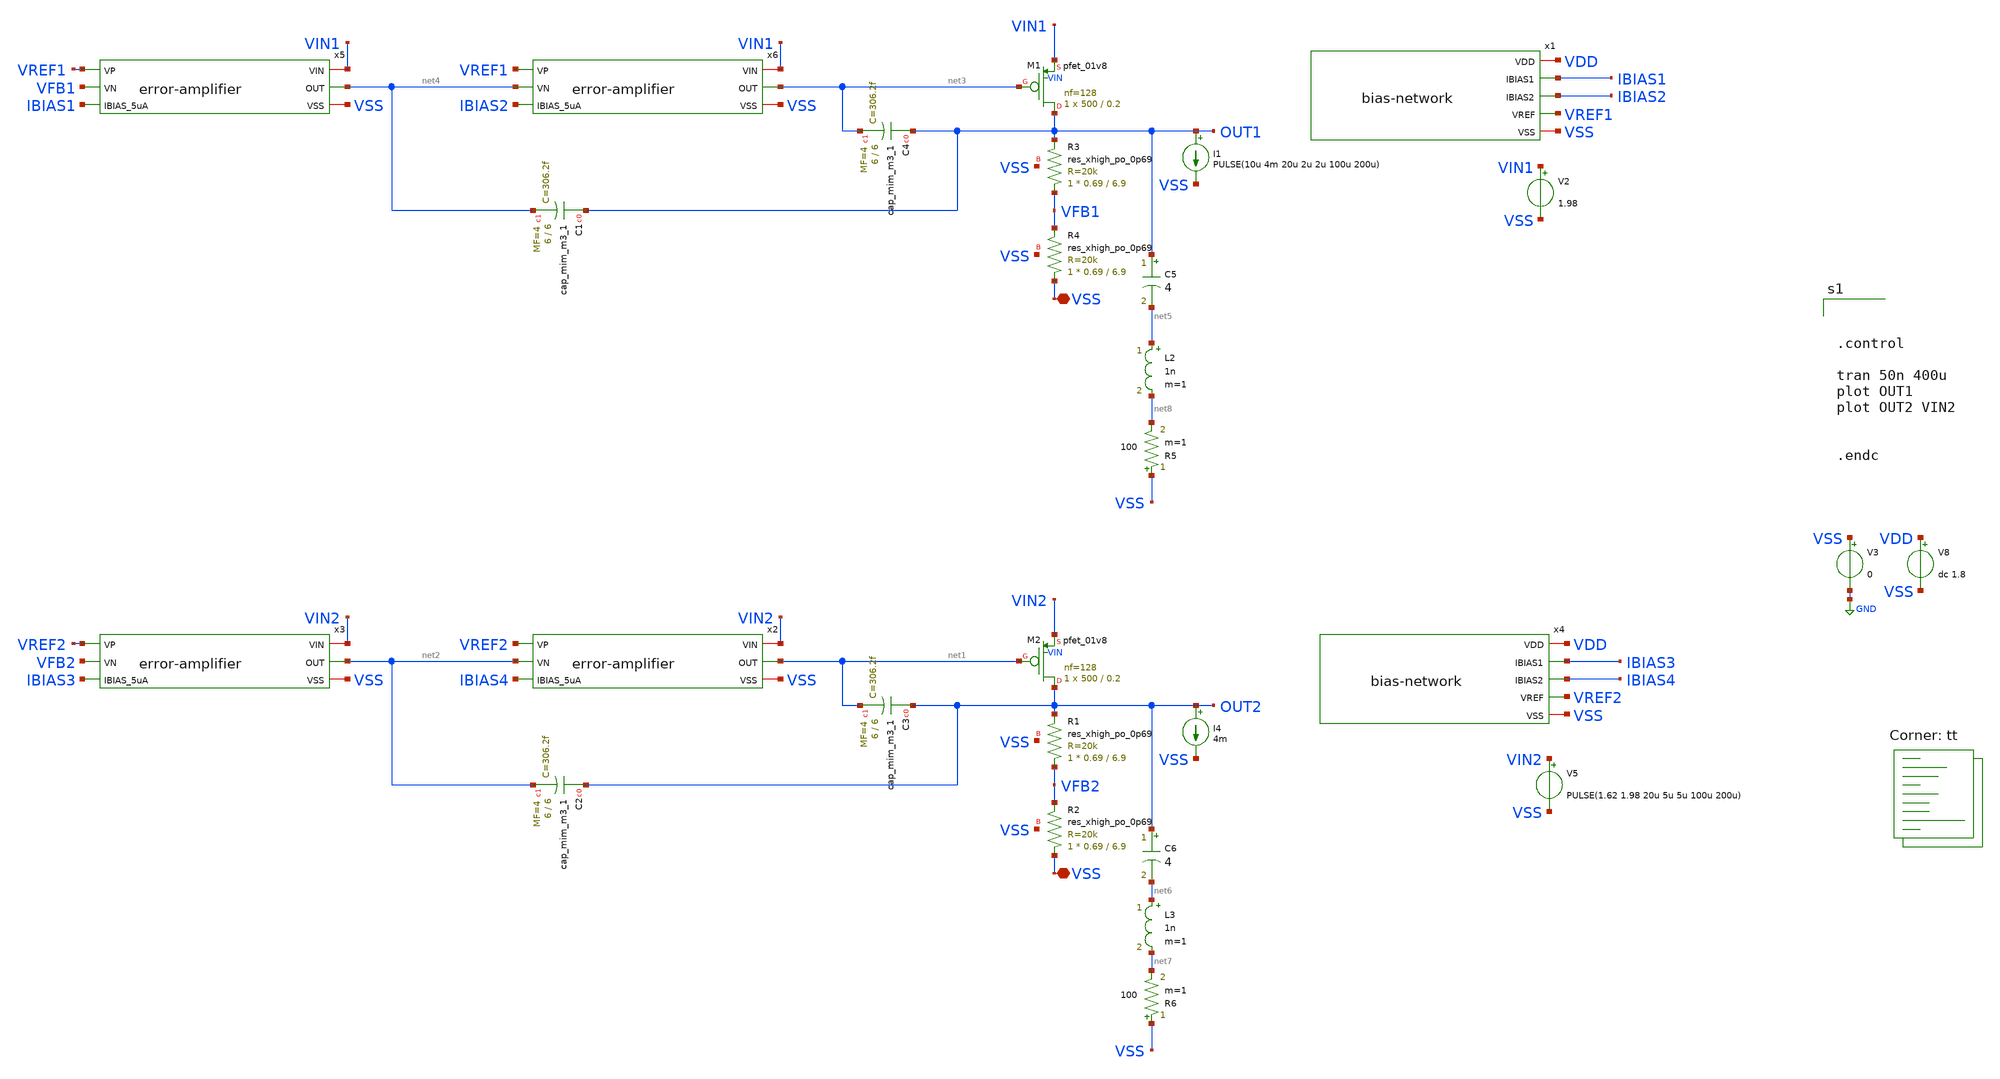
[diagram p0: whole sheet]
** sch_path: xschem/ldo_andriansyah/testbench/line-load-transient.sch
**.subckt line-load-transient VSS VSS
*.iopin VSS
*.iopin VSS
V2 VIN1 VSS 1.98
V3 VSS GND 0
I1 OUT1 VSS PULSE(10u 4m 20u 2u 2u 100u 200u)
V5 VIN2 VSS PULSE(1.62 1.98 20u 5u 5u 100u 200u)
I4 OUT2 VSS 4m
XC2 OUT2 net2 sky130_fd_pr__cap_mim_m3_1 W=6 L=6 MF=4 m=4
XC3 OUT2 net1 sky130_fd_pr__cap_mim_m3_1 W=6 L=6 MF=4 m=4
x3 VIN2 VREF2 VFB2 IBIAS3 net2 VSS error-amplifier
XR1 VFB2 OUT2 VSS sky130_fd_pr__res_xhigh_po_0p69 L=6.9 mult=1 m=1
XR2 VSS VFB2 VSS sky130_fd_pr__res_xhigh_po_0p69 L=6.9 mult=1 m=1
XM2 OUT2 net1 VIN2 VIN sky130_fd_pr__pfet_01v8 L=0.2 W=500 nf=128 ad='int((nf+1)/2) * W/nf * 0.29' as='int((nf+2)/2) * W/nf * 0.29'
+ pd='2*int((nf+1)/2) * (W/nf + 0.29)' ps='2*int((nf+2)/2) * (W/nf + 0.29)' nrd='0.29 / W' nrs='0.29 / W'
+ sa=0 sb=0 sd=0 mult=1 m=1
x2 VIN2 VREF2 net2 IBIAS4 net1 VSS error-amplifier
XC1 OUT1 net4 sky130_fd_pr__cap_mim_m3_1 W=6 L=6 MF=4 m=4
XC4 OUT1 net3 sky130_fd_pr__cap_mim_m3_1 W=6 L=6 MF=4 m=4
x5 VIN1 VREF1 VFB1 IBIAS1 net4 VSS error-amplifier
XR3 VFB1 OUT1 VSS sky130_fd_pr__res_xhigh_po_0p69 L=6.9 mult=1 m=1
XR4 VSS VFB1 VSS sky130_fd_pr__res_xhigh_po_0p69 L=6.9 mult=1 m=1
XM1 OUT1 net3 VIN1 VIN sky130_fd_pr__pfet_01v8 L=0.2 W=500 nf=128 ad='int((nf+1)/2) * W/nf * 0.29' as='int((nf+2)/2) * W/nf * 0.29'
+ pd='2*int((nf+1)/2) * (W/nf + 0.29)' ps='2*int((nf+2)/2) * (W/nf + 0.29)' nrd='0.29 / W' nrs='0.29 / W'
+ sa=0 sb=0 sd=0 mult=1 m=1
x6 VIN1 VREF1 net4 IBIAS2 net3 VSS error-amplifier
x1 VDD IBIAS1 IBIAS2 VREF1 VSS bias-network
x4 VDD IBIAS3 IBIAS4 VREF2 VSS bias-network
V8 VDD VSS dc 1.8
R5 VSS net8 100 m=1
C5 OUT1 net5 4 m=1
R6 VSS net7 100 m=1
C6 OUT2 net6 4 m=1
L2 net5 net8 1n m=1
L3 net6 net7 1n m=1
**** begin user architecture code



.control

tran 50n 400u
plot OUT1
plot OUT2 VIN2


.endc




.lib $::SKYWATER_MODELS/sky130.lib.spice tt
**** end user architecture code
**.ends

* expanding   symbol:
*+  /foss/designs/2026/tt_sky26b_ldo_andriansyah/xschem/error-amplifier/error-amplifier.sym # of pins=6
** sym_path: xschem/error-amplifier/error-amplifier.sym
** sch_path: xschem/error-amplifier/error-amplifier.sch
.subckt error-amplifier VIN VP VN IBIAS_5uA OUT VSS
*.ipin IBIAS_5uA
*.ipin VN
*.ipin VP
*.iopin VIN
*.iopin VSS
*.opin OUT
XM1 net2 net2 VSS VSS sky130_fd_pr__nfet_01v8 L=0.6 W=4.2 nf=4 ad='int((nf+1)/2) * W/nf * 0.29' as='int((nf+2)/2) * W/nf * 0.29'
+ pd='2*int((nf+1)/2) * (W/nf + 0.29)' ps='2*int((nf+2)/2) * (W/nf + 0.29)' nrd='0.29 / W' nrs='0.29 / W'
+ sa=0 sb=0 sd=0 mult=1 m=1
XM2 OUT net2 VSS VSS sky130_fd_pr__nfet_01v8 L=0.6 W=4.2 nf=4 ad='int((nf+1)/2) * W/nf * 0.29' as='int((nf+2)/2) * W/nf * 0.29'
+ pd='2*int((nf+1)/2) * (W/nf + 0.29)' ps='2*int((nf+2)/2) * (W/nf + 0.29)' nrd='0.29 / W' nrs='0.29 / W'
+ sa=0 sb=0 sd=0 mult=1 m=1
XM3 net2 VN net1 VIN sky130_fd_pr__pfet_01v8 L=0.6 W=28 nf=4 ad='int((nf+1)/2) * W/nf * 0.29' as='int((nf+2)/2) * W/nf * 0.29'
+ pd='2*int((nf+1)/2) * (W/nf + 0.29)' ps='2*int((nf+2)/2) * (W/nf + 0.29)' nrd='0.29 / W' nrs='0.29 / W'
+ sa=0 sb=0 sd=0 mult=1 m=1
XM4 OUT VP net1 VIN sky130_fd_pr__pfet_01v8 L=0.6 W=28 nf=4 ad='int((nf+1)/2) * W/nf * 0.29' as='int((nf+2)/2) * W/nf * 0.29'
+ pd='2*int((nf+1)/2) * (W/nf + 0.29)' ps='2*int((nf+2)/2) * (W/nf + 0.29)' nrd='0.29 / W' nrs='0.29 / W'
+ sa=0 sb=0 sd=0 mult=1 m=1
XM5 net1 IBIAS_5uA VIN VIN sky130_fd_pr__pfet_01v8 L=0.6 W=6.6 nf=4 ad='int((nf+1)/2) * W/nf * 0.29'
+ as='int((nf+2)/2) * W/nf * 0.29' pd='2*int((nf+1)/2) * (W/nf + 0.29)' ps='2*int((nf+2)/2) * (W/nf + 0.29)'
+ nrd='0.29 / W' nrs='0.29 / W' sa=0 sb=0 sd=0 mult=1 m=1
XM6 IBIAS_5uA IBIAS_5uA VIN VIN sky130_fd_pr__pfet_01v8 L=0.6 W=6.6 nf=4 ad='int((nf+1)/2) * W/nf * 0.29'
+ as='int((nf+2)/2) * W/nf * 0.29' pd='2*int((nf+1)/2) * (W/nf + 0.29)' ps='2*int((nf+2)/2) * (W/nf + 0.29)'
+ nrd='0.29 / W' nrs='0.29 / W' sa=0 sb=0 sd=0 mult=1 m=1
.ends


* expanding   symbol:
*+  /foss/designs/2026/tt_sky26b_ldo_andriansyah/xschem/bias-net/schematics/bias-network.sym # of pins=5
** sym_path: xschem/bias-net/schematics/bias-network.sym
** sch_path: xschem/bias-net/schematics/bias-network.sch
.subckt bias-network VDD IBIAS1 IBIAS2 VREF VSS
*.iopin VDD
*.iopin VSS
*.opin IBIAS1
*.opin IBIAS2
*.opin VREF
XM2 VREF VREF VSS VSS sky130_fd_pr__nfet_01v8 L=2 W=3 nf=4 ad='int((nf+1)/2) * W/nf * 0.29' as='int((nf+2)/2) * W/nf * 0.29'
+ pd='2*int((nf+1)/2) * (W/nf + 0.29)' ps='2*int((nf+2)/2) * (W/nf + 0.29)' nrd='0.29 / W' nrs='0.29 / W'
+ sa=0 sb=0 sd=0 mult=2 m=2
XR1 VREF net1 VSS sky130_fd_pr__res_xhigh_po_0p69 L=6.9 mult=1 m=1
XR2 net2 net1 VSS sky130_fd_pr__res_xhigh_po_0p69 L=6.9 mult=1 m=1
XR3 net2 net3 VSS sky130_fd_pr__res_xhigh_po_0p69 L=6.9 mult=1 m=1
XR4 net4 net3 VSS sky130_fd_pr__res_xhigh_po_0p69 L=6.9 mult=1 m=1
XR5 net4 net5 VSS sky130_fd_pr__res_xhigh_po_0p69 L=6.9 mult=1 m=1
XR6 net9 net10 VSS sky130_fd_pr__res_xhigh_po_0p69 L=6.9 mult=1 m=1
XR7 net9 net8 VSS sky130_fd_pr__res_xhigh_po_0p69 L=6.9 mult=1 m=1
XR8 net7 net8 VSS sky130_fd_pr__res_xhigh_po_0p69 L=6.9 mult=1 m=1
XR9 net7 net6 VSS sky130_fd_pr__res_xhigh_po_0p69 L=6.9 mult=1 m=1
XR10 net5 net6 VSS sky130_fd_pr__res_xhigh_po_0p69 L=6.9 mult=1 m=1
XM1 IBIAS1 VREF VSS VSS sky130_fd_pr__nfet_01v8 L=2 W=3 nf=4 ad='int((nf+1)/2) * W/nf * 0.29' as='int((nf+2)/2) * W/nf * 0.29'
+ pd='2*int((nf+1)/2) * (W/nf + 0.29)' ps='2*int((nf+2)/2) * (W/nf + 0.29)' nrd='0.29 / W' nrs='0.29 / W'
+ sa=0 sb=0 sd=0 mult=2 m=2
XM3 IBIAS2 VREF VSS VSS sky130_fd_pr__nfet_01v8 L=2 W=3 nf=4 ad='int((nf+1)/2) * W/nf * 0.29' as='int((nf+2)/2) * W/nf * 0.29'
+ pd='2*int((nf+1)/2) * (W/nf + 0.29)' ps='2*int((nf+2)/2) * (W/nf + 0.29)' nrd='0.29 / W' nrs='0.29 / W'
+ sa=0 sb=0 sd=0 mult=2 m=2
XR11 net10 net11 VSS sky130_fd_pr__res_xhigh_po_0p69 L=6.9 mult=1 m=1
XR12 net12 net11 VSS sky130_fd_pr__res_xhigh_po_0p69 L=6.9 mult=1 m=1
XR13 net12 net13 VSS sky130_fd_pr__res_xhigh_po_0p69 L=6.9 mult=1 m=1
XR14 net14 net13 VSS sky130_fd_pr__res_xhigh_po_0p69 L=6.9 mult=1 m=1
XR15 net14 net15 VSS sky130_fd_pr__res_xhigh_po_0p69 L=6.9 mult=1 m=1
XR16 net19 VDD VSS sky130_fd_pr__res_xhigh_po_0p69 L=6.9 mult=1 m=1
XR17 net19 net18 VSS sky130_fd_pr__res_xhigh_po_0p69 L=6.9 mult=1 m=1
XR18 net17 net18 VSS sky130_fd_pr__res_xhigh_po_0p69 L=6.9 mult=1 m=1
XR19 net17 net16 VSS sky130_fd_pr__res_xhigh_po_0p69 L=6.9 mult=1 m=1
XR20 net15 net16 VSS sky130_fd_pr__res_xhigh_po_0p69 L=6.9 mult=1 m=1
XR21 VSS VSS VSS sky130_fd_pr__res_xhigh_po_0p69 L=6.9 mult=1 m=1
XR22 VSS VSS VSS sky130_fd_pr__res_xhigh_po_0p69 L=6.9 mult=1 m=1
.ends

.GLOBAL GND
.end
